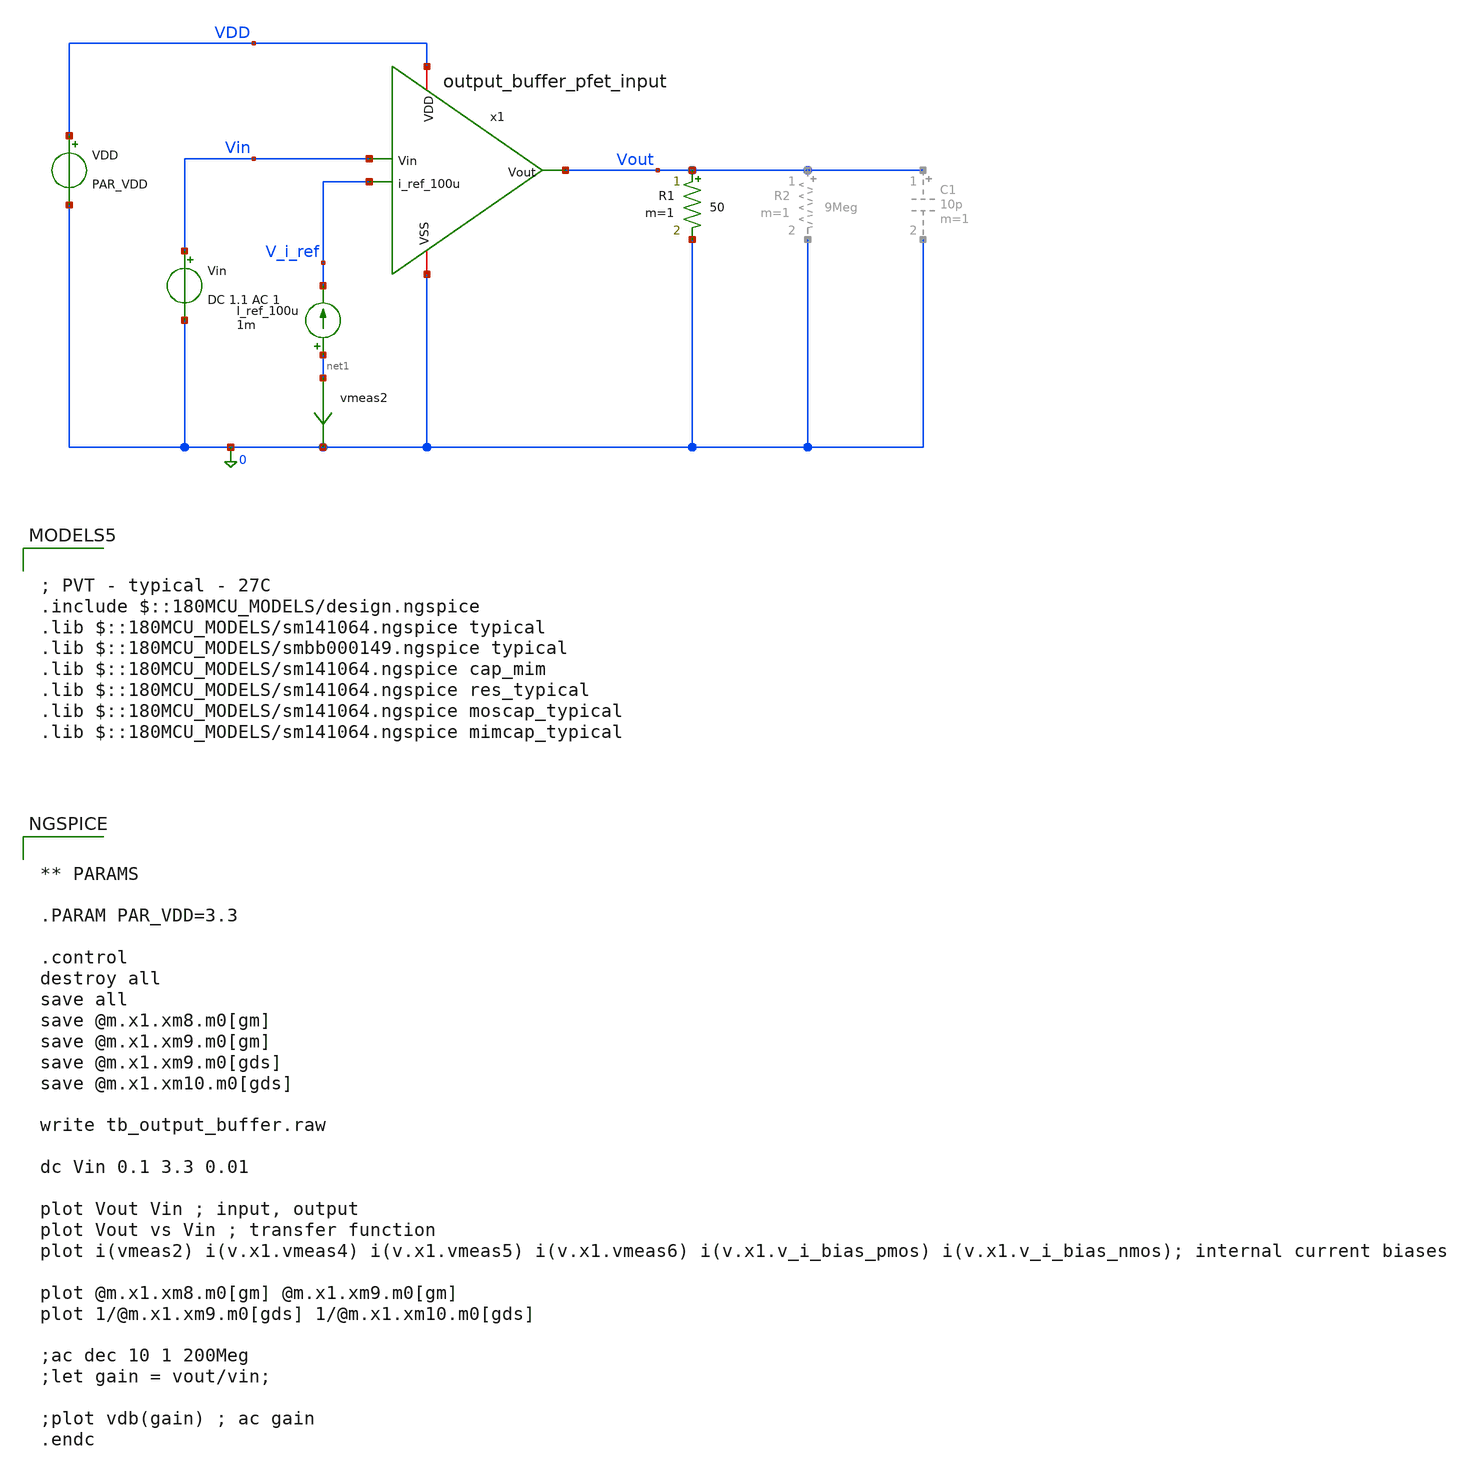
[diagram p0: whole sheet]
** sch_path: designs/output_buffer/testbench/tb_output_buffer_pfet_input.sch
**.subckt tb_output_buffer_pfet_input
I_ref_100u net1 V_i_ref 1m
Vin Vin 0 DC 1.1 AC 1
VDD VDD 0 PAR_VDD
R1 Vout 0 50 m=1
vmeas2 net1 0 0
.save i(vmeas2)
x1 Vout Vin V_i_ref VDD 0 output_buffer_pfet_input
**** begin user architecture code

; PVT - typical - 27C
.include $::180MCU_MODELS/design.ngspice
.lib $::180MCU_MODELS/sm141064.ngspice typical
.lib $::180MCU_MODELS/smbb000149.ngspice typical
.lib $::180MCU_MODELS/sm141064.ngspice cap_mim
.lib $::180MCU_MODELS/sm141064.ngspice res_typical
.lib $::180MCU_MODELS/sm141064.ngspice moscap_typical
.lib $::180MCU_MODELS/sm141064.ngspice mimcap_typical



** PARAMS

.PARAM PAR_VDD=3.3

.control
destroy all
save all
save @m.x1.xm8.m0[gm]
save @m.x1.xm9.m0[gm]
save @m.x1.xm9.m0[gds]
save @m.x1.xm10.m0[gds]

write tb_output_buffer.raw

dc Vin 0.1 3.3 0.01

plot Vout Vin ; input, output
plot Vout vs Vin ; transfer function
plot i(vmeas2) i(v.x1.vmeas4) i(v.x1.vmeas5) i(v.x1.vmeas6) i(v.x1.v_i_bias_pmos)
+ i(v.x1.v_i_bias_nmos); internal current biases

plot @m.x1.xm8.m0[gm] @m.x1.xm9.m0[gm]
plot 1/@m.x1.xm9.m0[gds] 1/@m.x1.xm10.m0[gds]

;ac dec 10 1 200Meg
;let gain = vout/vin;

;plot vdb(gain) ; ac gain
.endc


**** end user architecture code
**.ends

* expanding   symbol:  output_buffer/schematic/output_buffer_pfet_input.sym # of pins=5
** sym_path: designs/output_buffer/schematic/output_buffer_pfet_input.sym
** sch_path: designs/output_buffer/schematic/output_buffer_pfet_input.sch
.subckt output_buffer_pfet_input Vout Vin i_ref_100u VDD VSS
*.ipin Vin
*.opin Vout
*.ipin i_ref_100u
*.iopin VDD
*.iopin VSS
XM8 net2 Vin net1 net1 pfet_03v3 L=0.28u W=80u nf=10 ad='int((nf+1)/2) * W/nf * 0.18u' as='int((nf+2)/2) * W/nf * 0.18u'
+ pd='2*int((nf+1)/2) * (W/nf + 0.18u)' ps='2*int((nf+2)/2) * (W/nf + 0.18u)' nrd='0.18u / W' nrs='0.18u / W'
+ sa=0 sb=0 sd=0 m=1
XM9 net5 net2 VSS VSS nfet_03v3 L=.28u W=45u nf=1 ad='int((nf+1)/2) * W/nf * 0.18u' as='int((nf+2)/2) * W/nf * 0.18u'
+ pd='2*int((nf+1)/2) * (W/nf + 0.18u)' ps='2*int((nf+2)/2) * (W/nf + 0.18u)' nrd='0.18u / W' nrs='0.18u / W'
+ sa=0 sb=0 sd=0 m=1
C2 net3 net2 10p m=1
XM10 net6 net3 VDD VDD pfet_03v3 L=1u W=100u nf=10 ad='int((nf+1)/2) * W/nf * 0.18u' as='int((nf+2)/2) * W/nf * 0.18u'
+ pd='2*int((nf+1)/2) * (W/nf + 0.18u)' ps='2*int((nf+2)/2) * (W/nf + 0.18u)' nrd='0.18u / W' nrs='0.18u / W'
+ sa=0 sb=0 sd=0 m=1
R2 net4 net3 10G m=1
XM11 net8 i_ref_100u VSS VSS nfet_03v3 L=1u W=50u nf=1 ad='int((nf+1)/2) * W/nf * 0.18u' as='int((nf+2)/2) * W/nf * 0.18u'
+ pd='2*int((nf+1)/2) * (W/nf + 0.18u)' ps='2*int((nf+2)/2) * (W/nf + 0.18u)' nrd='0.18u / W' nrs='0.18u / W'
+ sa=0 sb=0 sd=0 m=1
XM12 i_ref_100u i_ref_100u VSS VSS nfet_03v3 L=1u W=1u nf=1 ad='int((nf+1)/2) * W/nf * 0.18u' as='int((nf+2)/2) * W/nf * 0.18u'
+ pd='2*int((nf+1)/2) * (W/nf + 0.18u)' ps='2*int((nf+2)/2) * (W/nf + 0.18u)' nrd='0.18u / W' nrs='0.18u / W'
+ sa=0 sb=0 sd=0 m=1
XM13 net7 i_ref_100u VSS VSS nfet_03v3 L=1u W=5u nf=1 ad='int((nf+1)/2) * W/nf * 0.18u' as='int((nf+2)/2) * W/nf * 0.18u'
+ pd='2*int((nf+1)/2) * (W/nf + 0.18u)' ps='2*int((nf+2)/2) * (W/nf + 0.18u)' nrd='0.18u / W' nrs='0.18u / W'
+ sa=0 sb=0 sd=0 m=1
XM14 net4 net4 VDD VDD pfet_03v3 L=1u W=1u nf=1 ad='int((nf+1)/2) * W/nf * 0.18u' as='int((nf+2)/2) * W/nf * 0.18u'
+ pd='2*int((nf+1)/2) * (W/nf + 0.18u)' ps='2*int((nf+2)/2) * (W/nf + 0.18u)' nrd='0.18u / W' nrs='0.18u / W'
+ sa=0 sb=0 sd=0 m=1
Vmeas4 Vout net1 0
.save i(vmeas4)
vmeas5 net6 Vout 0
.save i(vmeas5)
vmeas6 Vout net5 0
.save i(vmeas6)
v_i_bias_pmos net4 net7 0
.save i(v_i_bias_pmos)
v_i_bias_nmos net2 net8 0
.save i(v_i_bias_nmos)
.ends

.end
